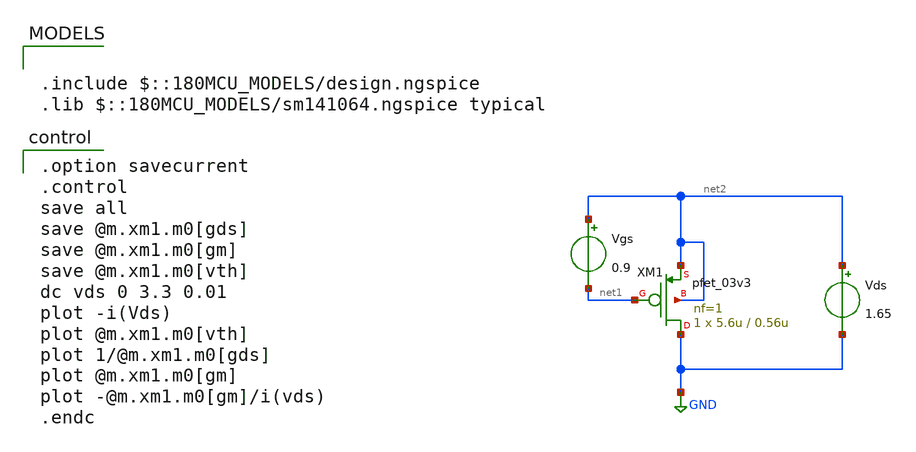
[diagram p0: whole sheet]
** sch_path: opamp/pfet_idvds_2L.sch
**.subckt pfet_idvds_2L
Vgs net2 net1 0.9
Vds net2 GND 1.65
XM1 GND net1 net2 net2 pfet_03v3 L=0.56u W=5.6u nf=1 ad='int((nf+1)/2) * W/nf * 0.18u' as='int((nf+2)/2) * W/nf * 0.18u'
+ pd='2*int((nf+1)/2) * (W/nf + 0.18u)' ps='2*int((nf+2)/2) * (W/nf + 0.18u)' nrd='0.18u / W' nrs='0.18u / W'
+ sa=0 sb=0 sd=0 m=1
**** begin user architecture code

.include $::180MCU_MODELS/design.ngspice
.lib $::180MCU_MODELS/sm141064.ngspice typical


.option savecurrent
.control
save all
save @m.xm1.m0[gds]
save @m.xm1.m0[gm]
save @m.xm1.m0[vth]
dc vds 0 3.3 0.01
plot -i(Vds)
plot @m.xm1.m0[vth]
plot 1/@m.xm1.m0[gds]
plot @m.xm1.m0[gm]
plot -@m.xm1.m0[gm]/i(vds)
.endc

**** end user architecture code
**.ends
.GLOBAL GND
.end
